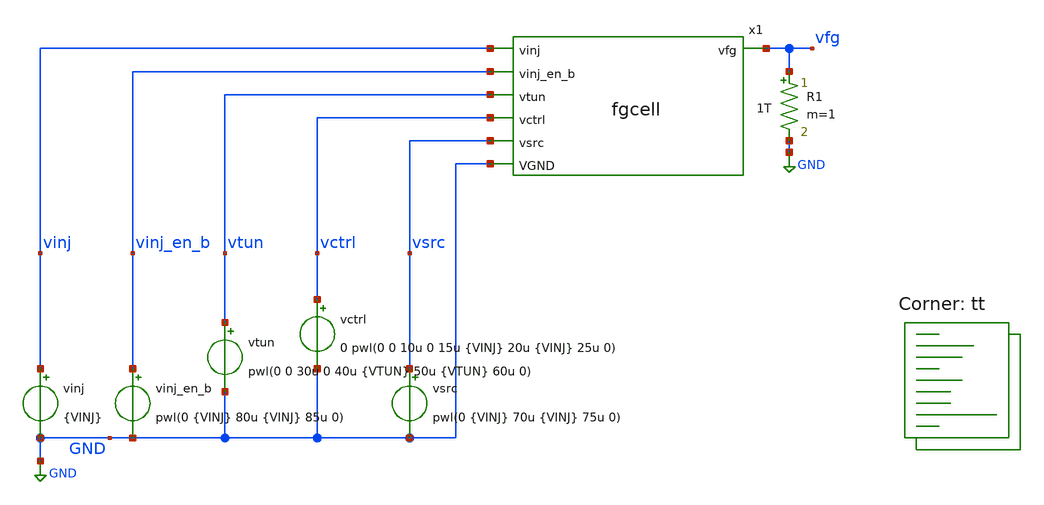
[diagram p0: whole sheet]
** sch_path: xschem/test-fgcell.sch
**.subckt test-fgcell
x1 vinj vinj_en_b vtun vctrl vsrc GND vfg fgcell
vinj_en_b vinj_en_b GND pwl(0 {VINJ} 80u {VINJ} 85u 0)
vctrl vctrl GND 0 pwl(0 0 10u 0 15u {VINJ} 20u {VINJ} 25u 0)
vsrc vsrc GND pwl(0 {VINJ} 70u {VINJ} 75u 0)
vtun vtun GND pwl(0 0 30u 0 40u {VTUN} 50u {VTUN} 60u 0)
vinj vinj GND {VINJ}
R1 vfg GND 1T m=1
**** begin user architecture code
.lib $::SKYWATER_MODELS/sky130.lib.spice tt



.options reltol=0.0001 abstol=10e-15 chgtol=1e-15
.include fgcell.spice
.param VTUN=12
.param VINJ=6
.param VDD=1.8
.param VSS=0
.option savecurrents
.ic v(vinj)=6 v(vinj_en_b)=6 v(vtun)=0 v(vsrc)=6 v(vfg)=0 v(x1.net1)=6
.control
  save all
  *op
  *remzerovec
  *write test-fgcell.raw
  *set appendwrite
  tran 10n 120u uic
  remzerovec
  write test-fgcell.raw
.endc



**** end user architecture code
**.ends
.GLOBAL GND
.end
